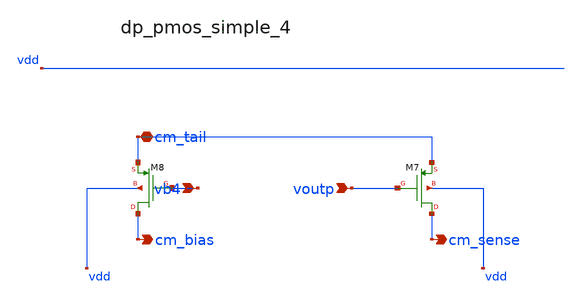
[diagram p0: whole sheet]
** sch_path: analog-db/raw/amp_027_fan_rrl_ota/hier/blocks/dp_pmos_simple_4.sch
**.subckt dp_pmos_simple_4 vb4 voutp cm_tail cm_bias cm_sense
*.ipin vb4
*.ipin voutp
*.iopin cm_tail
*.opin cm_bias
*.opin cm_sense
XM7 cm_sense voutp cm_tail vdd sg13_lv_pmos w=x_dut_xm7_w l=x_dut_xm7_l ng=1 m=x_dut_xm7_m
XM8 cm_bias vb4 cm_tail vdd sg13_lv_pmos w=x_dut_xm8_w l=x_dut_xm8_l ng=1 m=x_dut_xm8_m
**.ends
.end
